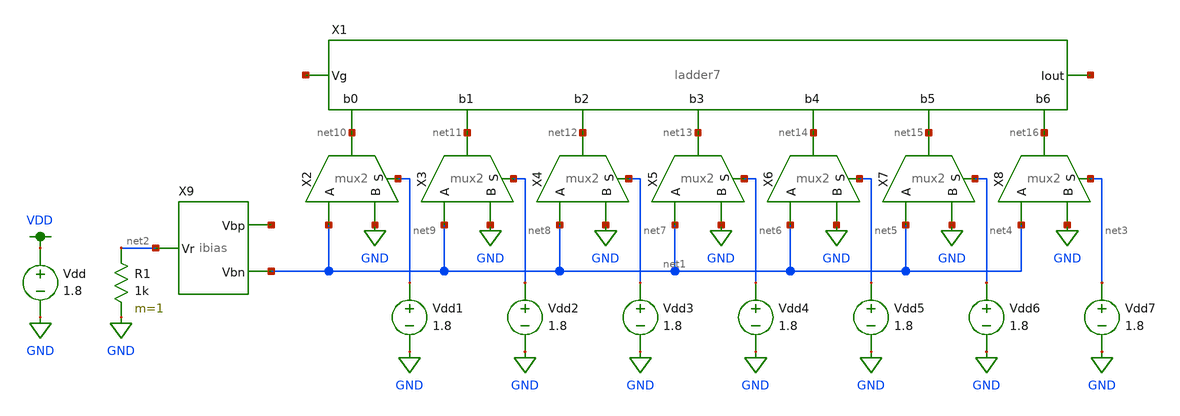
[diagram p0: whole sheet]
** sch_path: mini4/schem/ladder7_test.sch
**.subckt ladder7_test
X1 net10 net11 net12 net13 net14 net15 net16 net17 net18 ladder7
X2 net10 net1 GND net9 mux2
X3 net11 net1 GND net8 mux2
X4 net12 net1 GND net7 mux2
X5 net13 net1 GND net6 mux2
X6 net14 net1 GND net5 mux2
X7 net15 net1 GND net4 mux2
X8 net16 net1 GND net3 mux2
X9 net2 net1 net19 ibias
R1 net2 GND 1k m=1
Vdd VDD GND 1.8
Vdd1 net9 GND 1.8
Vdd2 net8 GND 1.8
Vdd3 net7 GND 1.8
Vdd4 net6 GND 1.8
Vdd5 net5 GND 1.8
Vdd6 net4 GND 1.8
Vdd7 net3 GND 1.8
**.ends
.GLOBAL GND
.GLOBAL VDD
.end
